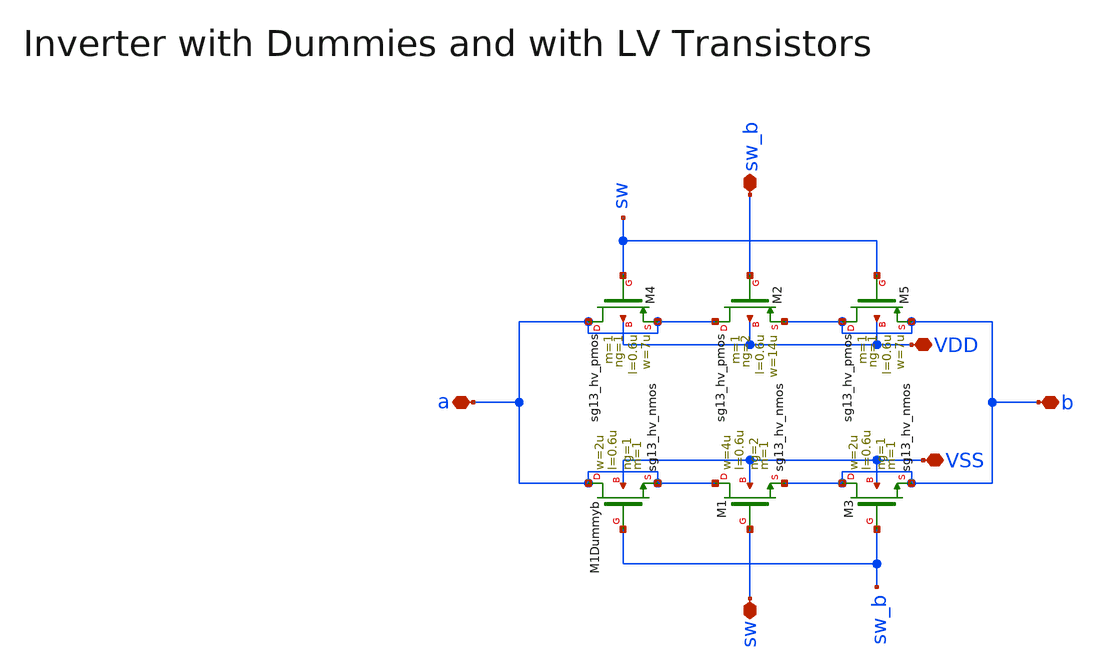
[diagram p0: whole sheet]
** sch_path: macros/heichips26_analog_project/macros/aswitch/schematic/xschem/aswitch.sch
**.subckt aswitch a sw_b b sw VDD VSS
*.iopin a
*.iopin sw_b
*.iopin b
*.iopin sw
*.iopin VDD
*.iopin VSS
XM1 a sw b VSS sg13_hv_nmos w=4u l=0.6u ng=2 m=1 mm_ok=1
XM2 a sw_b b VDD sg13_hv_pmos w=14u l=0.6u ng=2 m=1 mm_ok=1
XM1Dummyb a sw_b a VSS sg13_hv_nmos w=2u l=0.6u ng=1 m=1 mm_ok=1
XM3 b sw_b b VSS sg13_hv_nmos w=2u l=0.6u ng=1 m=1 mm_ok=1
XM4 a sw a VDD sg13_hv_pmos w=7u l=0.6u ng=1 m=1 mm_ok=1
XM5 b sw b VDD sg13_hv_pmos w=7u l=0.6u ng=1 m=1 mm_ok=1
**.ends
.end
